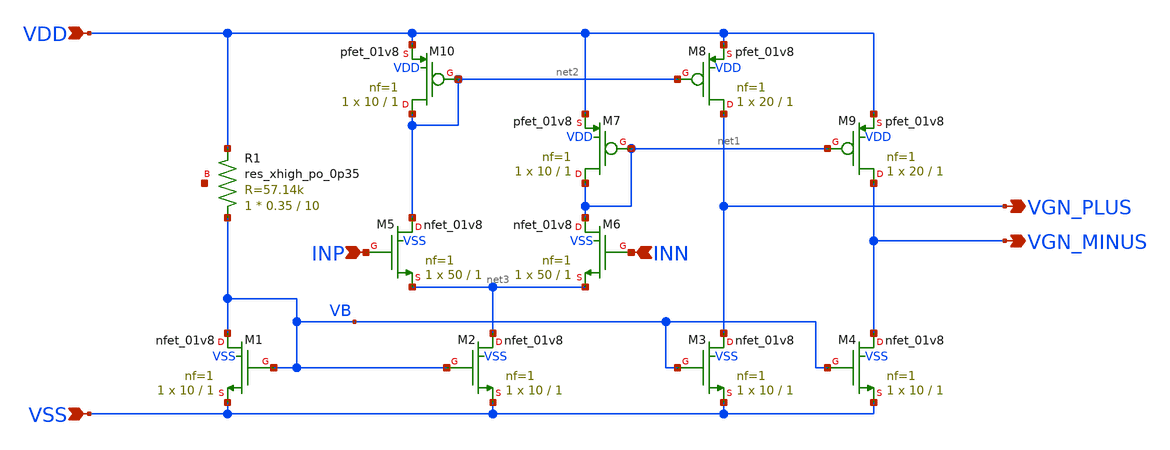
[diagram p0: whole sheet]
** sch_path: preamp.sch
**.subckt preamp VDD VSS INP INN VGN_PLUS VGN_MINUS
*.ipin VDD
*.ipin VSS
*.ipin INP
*.ipin INN
*.opin VGN_PLUS
*.opin VGN_MINUS
XM1 VB VB VSS VSS sky130_fd_pr__nfet_01v8 L=1 W=10 nf=1 ad='int((nf+1)/2) * W/nf * 0.29' as='int((nf+2)/2) * W/nf * 0.29'
+ pd='2*int((nf+1)/2) * (W/nf + 0.29)' ps='2*int((nf+2)/2) * (W/nf + 0.29)' nrd='0.29 / W' nrs='0.29 / W'
+ sa=0 sb=0 sd=0 mult=1 m=1
XM2 net3 VB VSS VSS sky130_fd_pr__nfet_01v8 L=1 W=10 nf=1 ad='int((nf+1)/2) * W/nf * 0.29' as='int((nf+2)/2) * W/nf * 0.29'
+ pd='2*int((nf+1)/2) * (W/nf + 0.29)' ps='2*int((nf+2)/2) * (W/nf + 0.29)' nrd='0.29 / W' nrs='0.29 / W'
+ sa=0 sb=0 sd=0 mult=1 m=1
XM3 VGN_PLUS VB VSS VSS sky130_fd_pr__nfet_01v8 L=1 W=10 nf=1 ad='int((nf+1)/2) * W/nf * 0.29' as='int((nf+2)/2) * W/nf * 0.29'
+ pd='2*int((nf+1)/2) * (W/nf + 0.29)' ps='2*int((nf+2)/2) * (W/nf + 0.29)' nrd='0.29 / W' nrs='0.29 / W'
+ sa=0 sb=0 sd=0 mult=1 m=1
XM4 VGN_MINUS VB VSS VSS sky130_fd_pr__nfet_01v8 L=1 W=10 nf=1 ad='int((nf+1)/2) * W/nf * 0.29' as='int((nf+2)/2) * W/nf * 0.29'
+ pd='2*int((nf+1)/2) * (W/nf + 0.29)' ps='2*int((nf+2)/2) * (W/nf + 0.29)' nrd='0.29 / W' nrs='0.29 / W'
+ sa=0 sb=0 sd=0 mult=1 m=1
XM5 net2 INP net3 VSS sky130_fd_pr__nfet_01v8 L=1 W=50 nf=1 ad='int((nf+1)/2) * W/nf * 0.29' as='int((nf+2)/2) * W/nf * 0.29'
+ pd='2*int((nf+1)/2) * (W/nf + 0.29)' ps='2*int((nf+2)/2) * (W/nf + 0.29)' nrd='0.29 / W' nrs='0.29 / W'
+ sa=0 sb=0 sd=0 mult=1 m=1
XM6 net1 INN net3 VSS sky130_fd_pr__nfet_01v8 L=1 W=50 nf=1 ad='int((nf+1)/2) * W/nf * 0.29' as='int((nf+2)/2) * W/nf * 0.29'
+ pd='2*int((nf+1)/2) * (W/nf + 0.29)' ps='2*int((nf+2)/2) * (W/nf + 0.29)' nrd='0.29 / W' nrs='0.29 / W'
+ sa=0 sb=0 sd=0 mult=1 m=1
XM7 net1 net1 VDD VDD sky130_fd_pr__pfet_01v8 L=1 W=10 nf=1 ad='int((nf+1)/2) * W/nf * 0.29' as='int((nf+2)/2) * W/nf * 0.29'
+ pd='2*int((nf+1)/2) * (W/nf + 0.29)' ps='2*int((nf+2)/2) * (W/nf + 0.29)' nrd='0.29 / W' nrs='0.29 / W'
+ sa=0 sb=0 sd=0 mult=1 m=1
XM8 VGN_PLUS net2 VDD VDD sky130_fd_pr__pfet_01v8 L=1 W=20 nf=1 ad='int((nf+1)/2) * W/nf * 0.29' as='int((nf+2)/2) * W/nf * 0.29'
+ pd='2*int((nf+1)/2) * (W/nf + 0.29)' ps='2*int((nf+2)/2) * (W/nf + 0.29)' nrd='0.29 / W' nrs='0.29 / W'
+ sa=0 sb=0 sd=0 mult=1 m=1
XM9 VGN_MINUS net1 VDD VDD sky130_fd_pr__pfet_01v8 L=1 W=20 nf=1 ad='int((nf+1)/2) * W/nf * 0.29' as='int((nf+2)/2) * W/nf * 0.29'
+ pd='2*int((nf+1)/2) * (W/nf + 0.29)' ps='2*int((nf+2)/2) * (W/nf + 0.29)' nrd='0.29 / W' nrs='0.29 / W'
+ sa=0 sb=0 sd=0 mult=1 m=1
XM10 net2 net2 VDD VDD sky130_fd_pr__pfet_01v8 L=1 W=10 nf=1 ad='int((nf+1)/2) * W/nf * 0.29' as='int((nf+2)/2) * W/nf * 0.29'
+ pd='2*int((nf+1)/2) * (W/nf + 0.29)' ps='2*int((nf+2)/2) * (W/nf + 0.29)' nrd='0.29 / W' nrs='0.29 / W'
+ sa=0 sb=0 sd=0 mult=1 m=1
XR1 VB VDD net4 sky130_fd_pr__res_xhigh_po_0p35 L=10 mult=1 m=1
**.ends
.end
